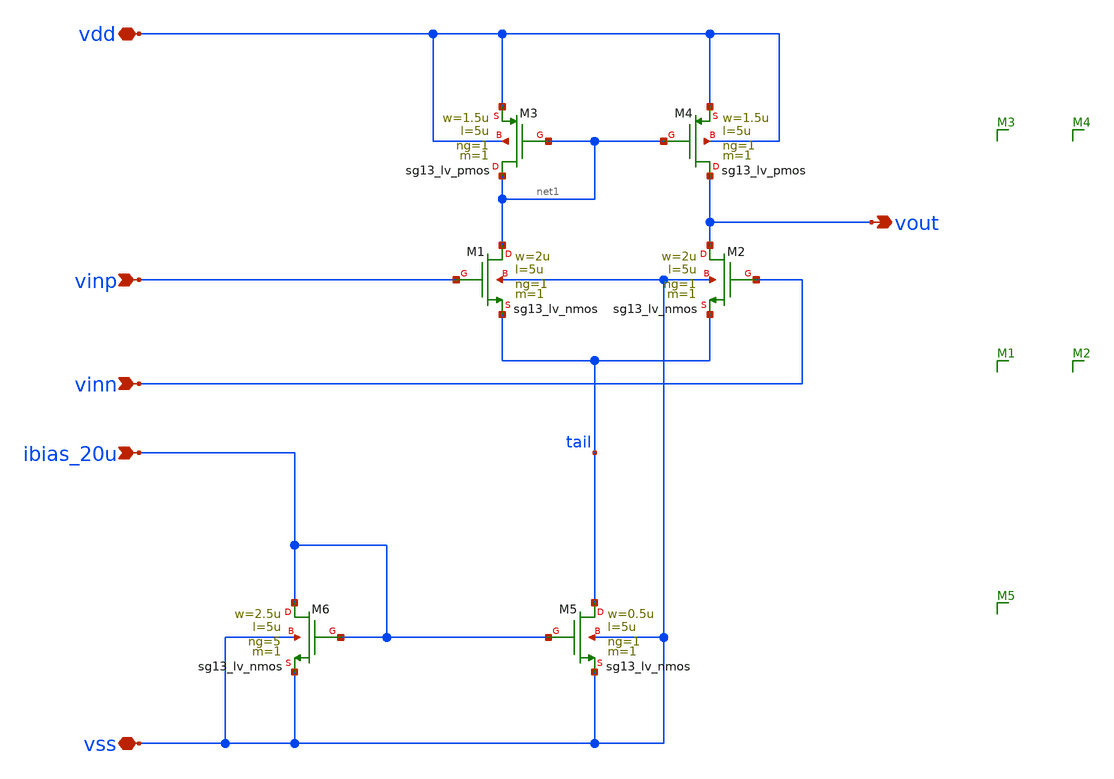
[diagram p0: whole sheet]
** sch_path: Modulo_Analogico/Lab8/ota-5t.sch
* (c) 2024-2025 Harald Pretl, Apache-2.0 license
**.subckt ota-5t ibias_20u vdd vss vinp vinn vout
*.ipin ibias_20u
*.iopin vdd
*.iopin vss
*.ipin vinp
*.ipin vinn
*.opin vout
XM5 tail ibias_20u vss vss sg13_lv_nmos w=0.5u l=5u ng=1 m=1 mm_ok=1
XM4 vout net1 vdd vdd sg13_lv_pmos w=1.5u l=5u ng=1 m=1 mm_ok=1
XM1 net1 vinp tail vss sg13_lv_nmos w=2u l=5u ng=1 m=1 mm_ok=1
XM2 vout vinn tail vss sg13_lv_nmos w=2u l=5u ng=1 m=1 mm_ok=1
XM3 net1 net1 vdd vdd sg13_lv_pmos w=1.5u l=5u ng=1 m=1 mm_ok=1
XM6 ibias_20u ibias_20u vss vss sg13_lv_nmos w=2.5u l=5u ng=5 m=1 mm_ok=1
**.ends
.end
